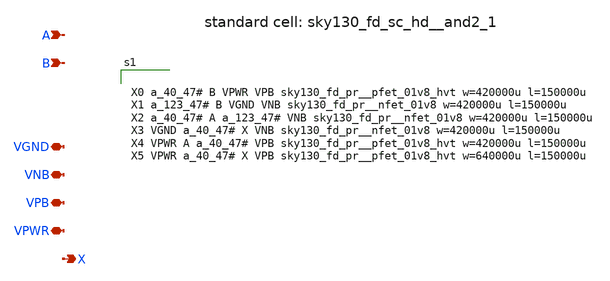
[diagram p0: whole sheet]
** sch_path: tt_um_mosbius/xschem/and.sch
**.subckt and A B VGND VNB VPB VPWR X
*.ipin A
*.ipin B
*.iopin VGND
*.iopin VNB
*.iopin VPB
*.iopin VPWR
*.opin X
**** begin user architecture code


X0 a_40_47# B VPWR VPB sky130_fd_pr__pfet_01v8_hvt w=420000u l=150000u
X1 a_123_47# B VGND VNB sky130_fd_pr__nfet_01v8 w=420000u l=150000u
X2 a_40_47# A a_123_47# VNB sky130_fd_pr__nfet_01v8 w=420000u l=150000u
X3 VGND a_40_47# X VNB sky130_fd_pr__nfet_01v8 w=420000u l=150000u
X4 VPWR A a_40_47# VPB sky130_fd_pr__pfet_01v8_hvt w=420000u l=150000u
X5 VPWR a_40_47# X VPB sky130_fd_pr__pfet_01v8_hvt w=640000u l=150000u




**** end user architecture code
**.ends
.end
